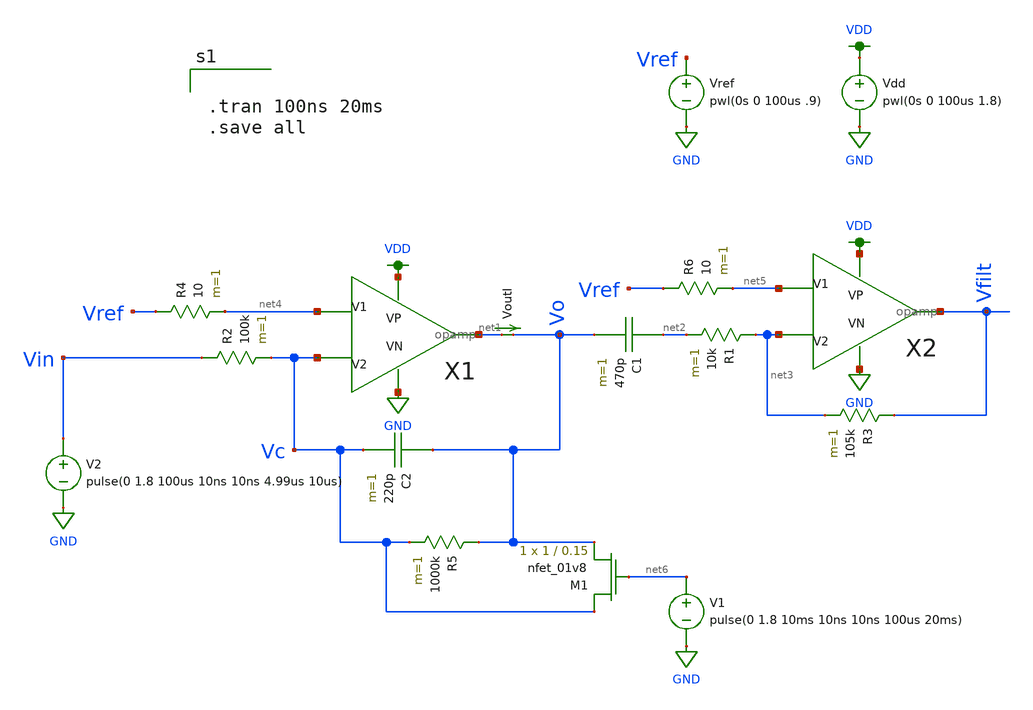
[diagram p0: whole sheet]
** sch_path: schematics/opamp_testbench.sch
**.subckt opamp_testbench
Vdd VDD GND pwl(0s 0 100us 1.8)
X1 net4 Vc VDD GND net1 opamp
VoutI net1 Vo 0
.save i(vouti)
V2 Vin GND pulse(0 1.8 100us 10ns 10ns 4.99us 10us)
R2 Vin Vc 100k m=1
Vref Vref GND pwl(0s 0 100us .9)
C2 Vo Vc 220p m=1
X2 net5 net3 VDD GND Vfilt opamp
C1 net2 Vo 470p m=1
R1 net3 net2 10k m=1
R3 Vfilt net3 105k m=1
R4 Vref net4 10 m=1
R5 Vo Vc 1000k m=1
R6 Vref net5 10 m=1
V1 net6 GND pulse(0 1.8 10ms 10ns 10ns 100us 20ms)
XM1 Vc net6 Vo GND sky130_fd_pr__nfet_01v8 L=0.15 W=1 nf=1 ad='int((nf+1)/2) * W/nf * 0.29' as='int((nf+2)/2) * W/nf * 0.29'
+ pd='2*int((nf+1)/2) * (W/nf + 0.29)' ps='2*int((nf+2)/2) * (W/nf + 0.29)' nrd='0.29 / W' nrs='0.29 / W'
+ sa=0 sb=0 sd=0 mult=1 m=1
**** begin user architecture code

.option wnflag=1
.param MC_SWITCH=0.0
.lib ~/skywater/skywater-pdk/libraries/sky130_fd_pr_ngspice/latest/models/sky130.lib.spice tt



.tran 100ns 20ms
.save all

**** end user architecture code
**.ends

* expanding   symbol:  /home/madvlsi/Documents/MADVLSI_final/schematics/opamp.sym # of pins=5
** sym_path: schematics/opamp.sym
** sch_path: schematics/opamp.sch
.subckt opamp V1 V2 VP VN Vout
*.ipin V1
*.ipin V2
*.opin Vout
*.iopin VP
*.iopin VN
*.iopin VP
*.iopin VN
XM1 VN net7 net2 GND sky130_fd_pr__nfet_01v8 L=l W=w nf=1 ad='int((nf+1)/2) * W/nf * 0.29' as='int((nf+2)/2) * W/nf * 0.29'
+ pd='2*int((nf+1)/2) * (W/nf + 0.29)' ps='2*int((nf+2)/2) * (W/nf + 0.29)' nrd='0.29 / W' nrs='0.29 / W'
+ sa=0 sb=0 sd=0 mult=1 m=1
XM2 VP net3 net1 VDD sky130_fd_pr__pfet_01v8 L=l W=w nf=1 ad='int((nf+1)/2) * W/nf * 0.29' as='int((nf+2)/2) * W/nf * 0.29'
+ pd='2*int((nf+1)/2) * (W/nf + 0.29)' ps='2*int((nf+2)/2) * (W/nf + 0.29)' nrd='0.29 / W' nrs='0.29 / W'
+ sa=0 sb=0 sd=0 mult=1 m=1
XM3 net1 V1 Vd VDD sky130_fd_pr__pfet_01v8 L=l W=w nf=1 ad='int((nf+1)/2) * W/nf * 0.29' as='int((nf+2)/2) * W/nf * 0.29'
+ pd='2*int((nf+1)/2) * (W/nf + 0.29)' ps='2*int((nf+2)/2) * (W/nf + 0.29)' nrd='0.29 / W' nrs='0.29 / W'
+ sa=0 sb=0 sd=0 mult=1 m=1
XM4 Vc V2 net1 VDD sky130_fd_pr__pfet_01v8 L=l W=w nf=1 ad='int((nf+1)/2) * W/nf * 0.29' as='int((nf+2)/2) * W/nf * 0.29'
+ pd='2*int((nf+1)/2) * (W/nf + 0.29)' ps='2*int((nf+2)/2) * (W/nf + 0.29)' nrd='0.29 / W' nrs='0.29 / W'
+ sa=0 sb=0 sd=0 mult=1 m=1
XM5 Va V2 net2 GND sky130_fd_pr__nfet_01v8 L=l W=w nf=1 ad='int((nf+1)/2) * W/nf * 0.29' as='int((nf+2)/2) * W/nf * 0.29'
+ pd='2*int((nf+1)/2) * (W/nf + 0.29)' ps='2*int((nf+2)/2) * (W/nf + 0.29)' nrd='0.29 / W' nrs='0.29 / W'
+ sa=0 sb=0 sd=0 mult=1 m=1
XM6 net2 V1 Vb GND sky130_fd_pr__nfet_01v8 L=l W=w nf=1 ad='int((nf+1)/2) * W/nf * 0.29' as='int((nf+2)/2) * W/nf * 0.29'
+ pd='2*int((nf+1)/2) * (W/nf + 0.29)' ps='2*int((nf+2)/2) * (W/nf + 0.29)' nrd='0.29 / W' nrs='0.29 / W'
+ sa=0 sb=0 sd=0 mult=1 m=1
XM7 net3 net3 Va VDD sky130_fd_pr__pfet_01v8 L=l W=w nf=1 ad='int((nf+1)/2) * W/nf * 0.29' as='int((nf+2)/2) * W/nf * 0.29'
+ pd='2*int((nf+1)/2) * (W/nf + 0.29)' ps='2*int((nf+2)/2) * (W/nf + 0.29)' nrd='0.29 / W' nrs='0.29 / W'
+ sa=0 sb=0 sd=0 mult=1 m=1
XM8 net6 net6 Va VDD sky130_fd_pr__pfet_01v8 L=l W=w nf=1 ad='int((nf+1)/2) * W/nf * 0.29' as='int((nf+2)/2) * W/nf * 0.29'
+ pd='2*int((nf+1)/2) * (W/nf + 0.29)' ps='2*int((nf+2)/2) * (W/nf + 0.29)' nrd='0.29 / W' nrs='0.29 / W'
+ sa=0 sb=0 sd=0 mult=1 m=1
XM9 net5 net6 Vb VDD sky130_fd_pr__pfet_01v8 L=l W=w nf=1 ad='int((nf+1)/2) * W/nf * 0.29' as='int((nf+2)/2) * W/nf * 0.29'
+ pd='2*int((nf+1)/2) * (W/nf + 0.29)' ps='2*int((nf+2)/2) * (W/nf + 0.29)' nrd='0.29 / W' nrs='0.29 / W'
+ sa=0 sb=0 sd=0 mult=1 m=1
XM10 Va net3 VP VDD sky130_fd_pr__pfet_01v8 L=l W=w nf=1 ad='int((nf+1)/2) * W/nf * 0.29' as='int((nf+2)/2) * W/nf * 0.29'
+ pd='2*int((nf+1)/2) * (W/nf + 0.29)' ps='2*int((nf+2)/2) * (W/nf + 0.29)' nrd='0.29 / W' nrs='0.29 / W'
+ sa=0 sb=0 sd=0 mult=1 m=1
XM11 Vb net3 VP VDD sky130_fd_pr__pfet_01v8 L=l W=w nf=1 ad='int((nf+1)/2) * W/nf * 0.29' as='int((nf+2)/2) * W/nf * 0.29'
+ pd='2*int((nf+1)/2) * (W/nf + 0.29)' ps='2*int((nf+2)/2) * (W/nf + 0.29)' nrd='0.29 / W' nrs='0.29 / W'
+ sa=0 sb=0 sd=0 mult=1 m=1
XM12 net6 net6 Vc GND sky130_fd_pr__nfet_01v8 L=l W=w nf=1 ad='int((nf+1)/2) * W/nf * 0.29' as='int((nf+2)/2) * W/nf * 0.29'
+ pd='2*int((nf+1)/2) * (W/nf + 0.29)' ps='2*int((nf+2)/2) * (W/nf + 0.29)' nrd='0.29 / W' nrs='0.29 / W'
+ sa=0 sb=0 sd=0 mult=1 m=1
XM13 net5 net6 Vd GND sky130_fd_pr__nfet_01v8 L=l W=w nf=1 ad='int((nf+1)/2) * W/nf * 0.29' as='int((nf+2)/2) * W/nf * 0.29'
+ pd='2*int((nf+1)/2) * (W/nf + 0.29)' ps='2*int((nf+2)/2) * (W/nf + 0.29)' nrd='0.29 / W' nrs='0.29 / W'
+ sa=0 sb=0 sd=0 mult=1 m=1
XM14 Vc net7 VN GND sky130_fd_pr__nfet_01v8 L=l W=w nf=1 ad='int((nf+1)/2) * W/nf * 0.29' as='int((nf+2)/2) * W/nf * 0.29'
+ pd='2*int((nf+1)/2) * (W/nf + 0.29)' ps='2*int((nf+2)/2) * (W/nf + 0.29)' nrd='0.29 / W' nrs='0.29 / W'
+ sa=0 sb=0 sd=0 mult=1 m=1
XM15 Vd net7 VN GND sky130_fd_pr__nfet_01v8 L=l W=w nf=1 ad='int((nf+1)/2) * W/nf * 0.29' as='int((nf+2)/2) * W/nf * 0.29'
+ pd='2*int((nf+1)/2) * (W/nf + 0.29)' ps='2*int((nf+2)/2) * (W/nf + 0.29)' nrd='0.29 / W' nrs='0.29 / W'
+ sa=0 sb=0 sd=0 mult=1 m=1
XM16 net8 net7 net3 GND sky130_fd_pr__nfet_01v8 L=l W=w nf=1 ad='int((nf+1)/2) * W/nf * 0.29' as='int((nf+2)/2) * W/nf * 0.29'
+ pd='2*int((nf+1)/2) * (W/nf + 0.29)' ps='2*int((nf+2)/2) * (W/nf + 0.29)' nrd='0.29 / W' nrs='0.29 / W'
+ sa=0 sb=0 sd=0 mult=1 m=1
XM17 VN net7 net8 GND sky130_fd_pr__nfet_01v8 L=l W=w nf=1 ad='int((nf+1)/2) * W/nf * 0.29' as='int((nf+2)/2) * W/nf * 0.29'
+ pd='2*int((nf+1)/2) * (W/nf + 0.29)' ps='2*int((nf+2)/2) * (W/nf + 0.29)' nrd='0.29 / W' nrs='0.29 / W'
+ sa=0 sb=0 sd=0 mult=1 m=1
XM18 net8 net7 VP GND sky130_fd_pr__nfet_01v8 L=l W=w nf=1 ad='int((nf+1)/2) * W/nf * 0.29' as='int((nf+2)/2) * W/nf * 0.29'
+ pd='2*int((nf+1)/2) * (W/nf + 0.29)' ps='2*int((nf+2)/2) * (W/nf + 0.29)' nrd='0.29 / W' nrs='0.29 / W'
+ sa=0 sb=0 sd=0 mult=M m=M
XM19 net4 net3 net7 VDD sky130_fd_pr__pfet_01v8 L=l W=w nf=1 ad='int((nf+1)/2) * W/nf * 0.29' as='int((nf+2)/2) * W/nf * 0.29'
+ pd='2*int((nf+1)/2) * (W/nf + 0.29)' ps='2*int((nf+2)/2) * (W/nf + 0.29)' nrd='0.29 / W' nrs='0.29 / W'
+ sa=0 sb=0 sd=0 mult=1 m=1
XM20 VP net3 net4 VDD sky130_fd_pr__pfet_01v8 L=l W=w nf=1 ad='int((nf+1)/2) * W/nf * 0.29' as='int((nf+2)/2) * W/nf * 0.29'
+ pd='2*int((nf+1)/2) * (W/nf + 0.29)' ps='2*int((nf+2)/2) * (W/nf + 0.29)' nrd='0.29 / W' nrs='0.29 / W'
+ sa=0 sb=0 sd=0 mult=1 m=1
XM21 net4 net3 VN VDD sky130_fd_pr__pfet_01v8 L=l W=w nf=1 ad='int((nf+1)/2) * W/nf * 0.29' as='int((nf+2)/2) * W/nf * 0.29'
+ pd='2*int((nf+1)/2) * (W/nf + 0.29)' ps='2*int((nf+2)/2) * (W/nf + 0.29)' nrd='0.29 / W' nrs='0.29 / W'
+ sa=0 sb=0 sd=0 mult=M m=M
XM22 net7 net7 Vc GND sky130_fd_pr__nfet_01v8 L=l W=w nf=1 ad='int((nf+1)/2) * W/nf * 0.29' as='int((nf+2)/2) * W/nf * 0.29'
+ pd='2*int((nf+1)/2) * (W/nf + 0.29)' ps='2*int((nf+2)/2) * (W/nf + 0.29)' nrd='0.29 / W' nrs='0.29 / W'
+ sa=0 sb=0 sd=0 mult=1 m=1
**** begin user architecture code

.param M=3
.param w=3
.param l=0.6


**** end user architecture code
XM23 Vout net5 VN GND sky130_fd_pr__nfet_01v8 L=.15 W=6 nf=1 ad='int((nf+1)/2) * W/nf * 0.29' as='int((nf+2)/2) * W/nf * 0.29'
+ pd='2*int((nf+1)/2) * (W/nf + 0.29)' ps='2*int((nf+2)/2) * (W/nf + 0.29)' nrd='0.29 / W' nrs='0.29 / W'
+ sa=0 sb=0 sd=0 mult=1 m=1
XM24 Vout net5 VP VDD sky130_fd_pr__pfet_01v8 L=.15 W=12 nf=1 ad='int((nf+1)/2) * W/nf * 0.29' as='int((nf+2)/2) * W/nf * 0.29'
+ pd='2*int((nf+1)/2) * (W/nf + 0.29)' ps='2*int((nf+2)/2) * (W/nf + 0.29)' nrd='0.29 / W' nrs='0.29 / W'
+ sa=0 sb=0 sd=0 mult=1 m=1
C1 Vout net5 500f m=1
.ends

.GLOBAL GND
.GLOBAL VDD
.end
